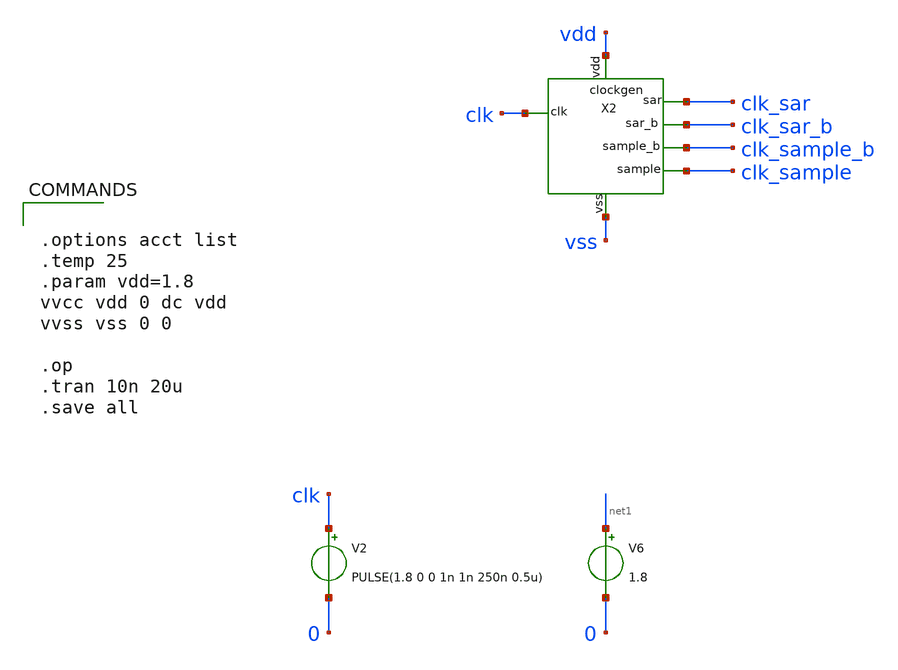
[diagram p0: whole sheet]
** sch_path: xschem/clockgen/clockgen_tb.sch
.lib $::SKYWATER_MODELS/sky130.lib.spice tt
.include $::SKYWATER_STDCELLS/sky130_fd_sc_hd.spice

**.subckt clockgen_tb
V2 clk 0 PULSE(1.8 0 0 1n 1n 250n 0.5u)
V6 net1 0 1.8
X2 clk vdd clk_sar clk_sample vss clk_sar_b clk_sample_b clockgen
**** begin user architecture code


.options acct list
.temp 25
.param vdd=1.8
vvcc vdd 0 dc vdd
vvss vss 0 0

.op
.tran 10n 20u
.save all


**** end user architecture code
**.ends

* expanding   symbol:  xschem/clockgen/clockgen.sym # of pins=7
** sym_path: xschem/clockgen/clockgen.sym
** sch_path: xschem/clockgen/clockgen.sch
.subckt clockgen clk vdd clk_sar clk_sample vss clk_sar_b clk_sample_b
*.opin clk_sar
*.opin clk_sample
*.ipin clk
*.iopin vss
*.iopin vdd
*.opin clk_sar_b
*.opin clk_sample_b
x1 clk vss clk_sample vss vss vdd vdd clk_sar sky130_fd_sc_hd__mux2_1
x8 net2 d1 net1 d3 vss vss vdd vdd clk_sample sky130_fd_sc_hd__and4_2
x14 clk net3 rst vss vss vdd vdd d0 net3 sky130_fd_sc_hd__dfrbp_2
x15 d1 d0 vss vss vdd vdd net4 sky130_fd_sc_hd__xor2_1
x16 clk net4 rst vss vss vdd vdd d1 net10 sky130_fd_sc_hd__dfrbp_2
x17 d1 d0 vss vss vdd vdd net7 sky130_fd_sc_hd__and2_1
x18 d2 net7 vss vss vdd vdd net5 sky130_fd_sc_hd__xor2_1
x20 d2 net7 vss vss vdd vdd net11 sky130_fd_sc_hd__and2_1
x21 d3 net11 vss vss vdd vdd net6 sky130_fd_sc_hd__xor2_1
x19 clk net5 rst vss vss vdd vdd d2 net12 sky130_fd_sc_hd__dfrbp_2
x22 clk net6 rst vss vss vdd vdd d3 net13 sky130_fd_sc_hd__dfrbp_2
x23 d0 vss vss vdd vdd net2 sky130_fd_sc_hd__inv_1
x25 d2 vss vss vdd vdd net1 sky130_fd_sc_hd__inv_1
x24 d1 d3 vss vss vdd vdd net9 sky130_fd_sc_hd__and2_1
x26 net9 vss vss vdd vdd net8 sky130_fd_sc_hd__inv_1
x27 clk net8 vss vss vdd vdd rst net14 sky130_fd_sc_hd__dfxbp_2
x2 clk_sar vss vss vdd vdd clk_sar_b sky130_fd_sc_hd__inv_1
x3 clk_sample vss vss vdd vdd clk_sample_b sky130_fd_sc_hd__inv_1
.ends

.end
